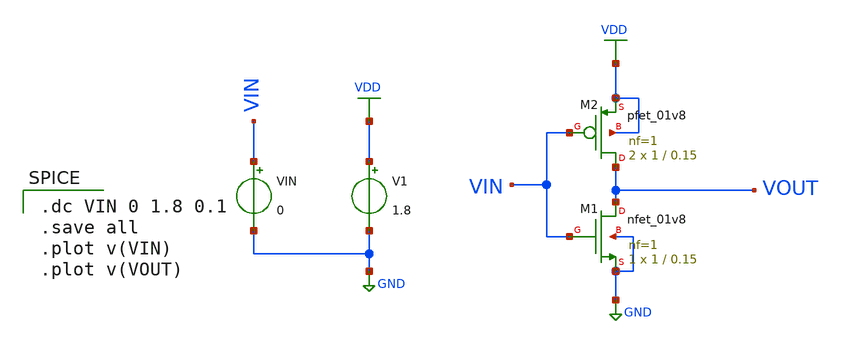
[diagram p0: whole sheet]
** sch_path: Circuits/Examples/Digital/NOT/NOT_GATE.sch
**.subckt NOT_GATE
XM1 VOUT VIN GND GND sky130_fd_pr__nfet_01v8 L=0.15 W=1 nf=1 ad='int((nf+1)/2) * W/nf * 0.29' as='int((nf+2)/2) * W/nf * 0.29'
+ pd='2*int((nf+1)/2) * (W/nf + 0.29)' ps='2*int((nf+2)/2) * (W/nf + 0.29)' nrd='0.29 / W' nrs='0.29 / W'
+ sa=0 sb=0 sd=0 mult=1 m=1
XM2 VOUT VIN VDD VDD sky130_fd_pr__pfet_01v8 L=0.15 W=1 nf=1 ad='int((nf+1)/2) * W/nf * 0.29' as='int((nf+2)/2) * W/nf * 0.29'
+ pd='2*int((nf+1)/2) * (W/nf + 0.29)' ps='2*int((nf+2)/2) * (W/nf + 0.29)' nrd='0.29 / W' nrs='0.29 / W'
+ sa=0 sb=0 sd=0 mult=2 m=2
V1 VDD GND 1.8
VIN VIN GND 0
**** begin user architecture code
 ** manual skywater pdks install (with patches applied)
* .lib $::SKYWATER_MODELS/models/sky130.lib.spice tt

** opencircuitdesign pdks install
.lib $::SKYWATER_MODELS/sky130.lib.spice tt

.param mc_mm_switch=0
.param mc_pr_switch=0


.dc VIN 0 1.8 0.1
.save all
.plot v(VIN)
.plot v(VOUT)

**** end user architecture code
**.ends
.GLOBAL VDD
.GLOBAL GND
.end
